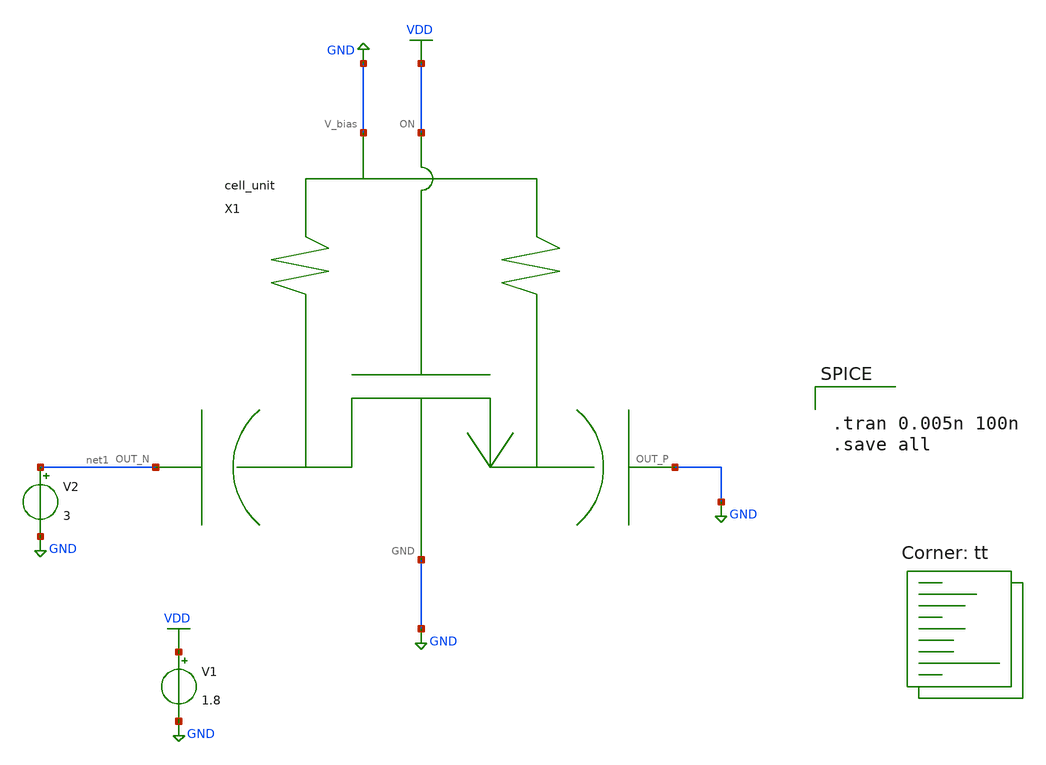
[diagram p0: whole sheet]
** sch_path: xschem/cell_unit_tb.sch
**.subckt cell_unit_tb
V1 VDD GND 1.8
X1 GND VDD net1 GND GND cell_unit
V2 net1 GND 3
**** begin user architecture code


.tran 0.005n 100n
.save all


.lib $::SKYWATER_MODELS/sky130.lib.spice tt
**** end user architecture code
**.ends
.GLOBAL GND
.GLOBAL VDD
.end
